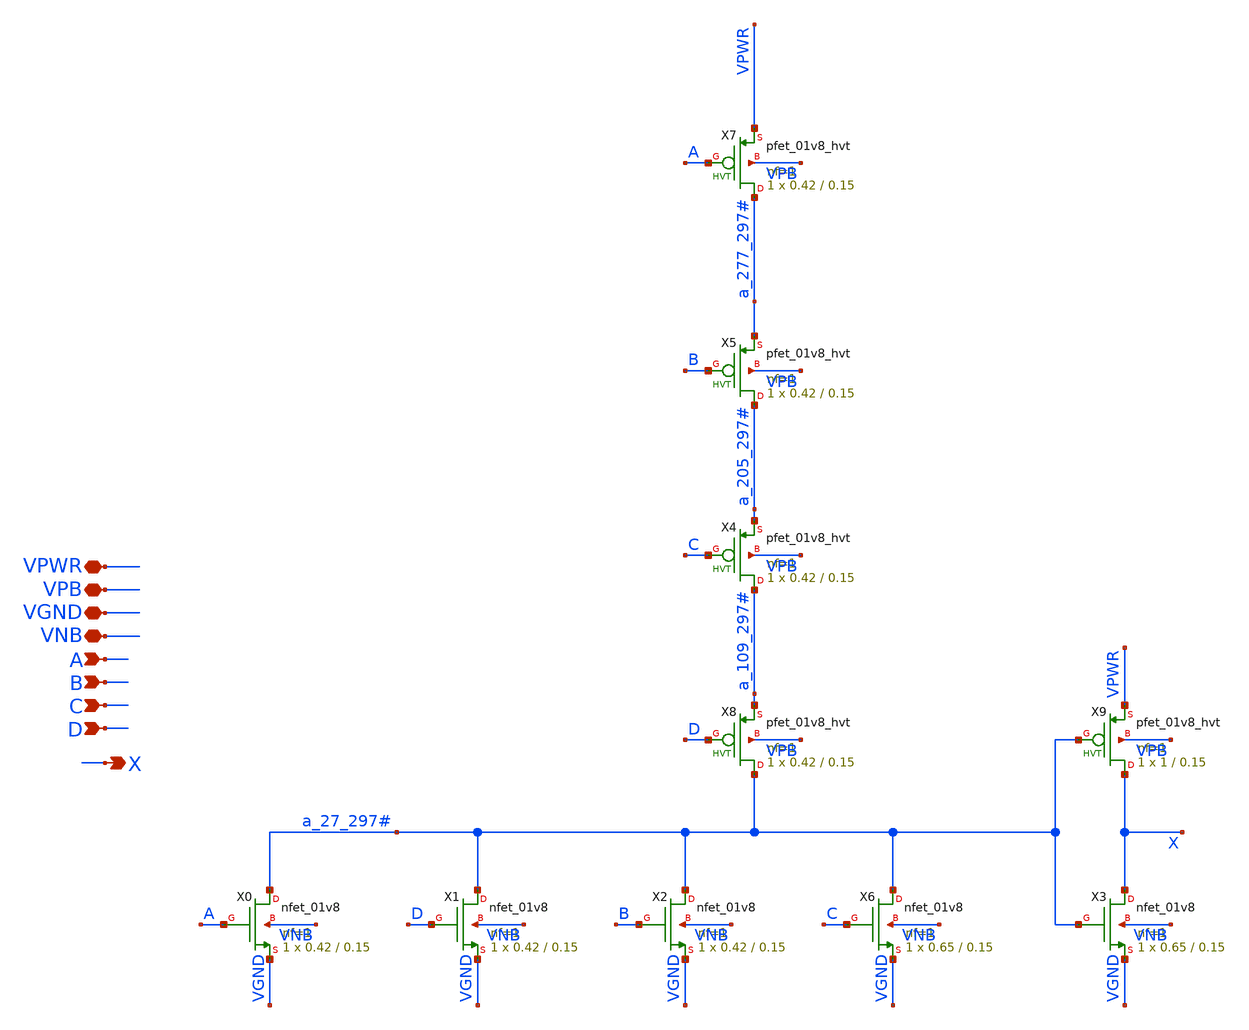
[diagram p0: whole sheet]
** sch_path: analog/klayout/production/final_merge_20260923/testbenches/cace/analog/xschem/sky130_fd_sc_hd__or4_1.sch
**.subckt sky130_fd_sc_hd__or4_1 A X VNB VPB VPWR D B C VGND
*.ipin A
*.opin X
*.iopin VNB
*.iopin VPB
*.iopin VPWR
*.ipin D
*.ipin B
*.ipin C
*.iopin VGND
XX0 a_27_297# A VGND VNB sky130_fd_pr__nfet_01v8 L=0.15 W=0.42 nf=1 ad='int((1 + 1)/2) * 0.42 / 1 * 0.29'
+ as='int((1 + 2)/2) * 0.42 / 1 * 0.29' pd='2*int((1 + 1)/2) * (0.42 / 1 + 0.29)' ps='2*int((1 + 2)/2) * (0.42 / 1 + 0.29)'
+ nrd='0.29 / 0.42 ' nrs='0.29 / 0.42 ' sa=0 sb=0 sd=0 mult=1 m=1
XX4 a_109_297# C a_205_297# VPB sky130_fd_pr__pfet_01v8_hvt L=0.15 W=0.42 nf=1 ad='int((1 + 1)/2) * 0.42 / 1 * 0.29'
+ as='int((1 + 2)/2) * 0.42 / 1 * 0.29' pd='2*int((1 + 1)/2) * (0.42 / 1 + 0.29)' ps='2*int((1 + 2)/2) * (0.42 / 1 + 0.29)'
+ nrd='0.29 / 0.42 ' nrs='0.29 / 0.42 ' sa=0 sb=0 sd=0 mult=1 m=1
XX1 a_27_297# D VGND VNB sky130_fd_pr__nfet_01v8 L=0.15 W=0.42 nf=1 ad='int((1 + 1)/2) * 0.42 / 1 * 0.29'
+ as='int((1 + 2)/2) * 0.42 / 1 * 0.29' pd='2*int((1 + 1)/2) * (0.42 / 1 + 0.29)' ps='2*int((1 + 2)/2) * (0.42 / 1 + 0.29)'
+ nrd='0.29 / 0.42 ' nrs='0.29 / 0.42 ' sa=0 sb=0 sd=0 mult=1 m=1
XX2 a_27_297# B VGND VNB sky130_fd_pr__nfet_01v8 L=0.15 W=0.42 nf=1 ad='int((1 + 1)/2) * 0.42 / 1 * 0.29'
+ as='int((1 + 2)/2) * 0.42 / 1 * 0.29' pd='2*int((1 + 1)/2) * (0.42 / 1 + 0.29)' ps='2*int((1 + 2)/2) * (0.42 / 1 + 0.29)'
+ nrd='0.29 / 0.42 ' nrs='0.29 / 0.42 ' sa=0 sb=0 sd=0 mult=1 m=1
XX3 X a_27_297# VGND VNB sky130_fd_pr__nfet_01v8 L=0.15 W=0.65 nf=1 ad='int((1 + 1)/2) * 0.65 / 1 * 0.29'
+ as='int((1 + 2)/2) * 0.65 / 1 * 0.29' pd='2*int((1 + 1)/2) * (0.65 / 1 + 0.29)' ps='2*int((1 + 2)/2) * (0.65 / 1 + 0.29)'
+ nrd='0.29 / 0.65 ' nrs='0.29 / 0.65 ' sa=0 sb=0 sd=0 mult=1 m=1
XX5 a_205_297# B a_277_297# VPB sky130_fd_pr__pfet_01v8_hvt L=0.15 W=0.42 nf=1 ad='int((1 + 1)/2) * 0.42 / 1 * 0.29'
+ as='int((1 + 2)/2) * 0.42 / 1 * 0.29' pd='2*int((1 + 1)/2) * (0.42 / 1 + 0.29)' ps='2*int((1 + 2)/2) * (0.42 / 1 + 0.29)'
+ nrd='0.29 / 0.42 ' nrs='0.29 / 0.42 ' sa=0 sb=0 sd=0 mult=1 m=1
XX6 a_27_297# C VGND VNB sky130_fd_pr__nfet_01v8 L=0.15 W=0.65 nf=1 ad='int((1 + 1)/2) * 0.65 / 1 * 0.29'
+ as='int((1 + 2)/2) * 0.65 / 1 * 0.29' pd='2*int((1 + 1)/2) * (0.65 / 1 + 0.29)' ps='2*int((1 + 2)/2) * (0.65 / 1 + 0.29)'
+ nrd='0.29 / 0.65 ' nrs='0.29 / 0.65 ' sa=0 sb=0 sd=0 mult=1 m=1
XX7 a_277_297# A VPWR VPB sky130_fd_pr__pfet_01v8_hvt L=0.15 W=0.42 nf=1 ad='int((1 + 1)/2) * 0.42 / 1 * 0.29'
+ as='int((1 + 2)/2) * 0.42 / 1 * 0.29' pd='2*int((1 + 1)/2) * (0.42 / 1 + 0.29)' ps='2*int((1 + 2)/2) * (0.42 / 1 + 0.29)'
+ nrd='0.29 / 0.42 ' nrs='0.29 / 0.42 ' sa=0 sb=0 sd=0 mult=1 m=1
XX8 a_27_297# D a_109_297# VPB sky130_fd_pr__pfet_01v8_hvt L=0.15 W=0.42 nf=1 ad='int((1 + 1)/2) * 0.42 / 1 * 0.29'
+ as='int((1 + 2)/2) * 0.42 / 1 * 0.29' pd='2*int((1 + 1)/2) * (0.42 / 1 + 0.29)' ps='2*int((1 + 2)/2) * (0.42 / 1 + 0.29)'
+ nrd='0.29 / 0.42 ' nrs='0.29 / 0.42 ' sa=0 sb=0 sd=0 mult=1 m=1
XX9 X a_27_297# VPWR VPB sky130_fd_pr__pfet_01v8_hvt L=0.15 W=1 nf=1 ad='int((1 + 1)/2) * 1 / 1 * 0.29'
+ as='int((1 + 2)/2) * 1 / 1 * 0.29' pd='2*int((1 + 1)/2) * (1 / 1 + 0.29)' ps='2*int((1 + 2)/2) * (1 / 1 + 0.29)'
+ nrd='0.29 / 1 ' nrs='0.29 / 1 ' sa=0 sb=0 sd=0 mult=1 m=1
**.ends
.end
